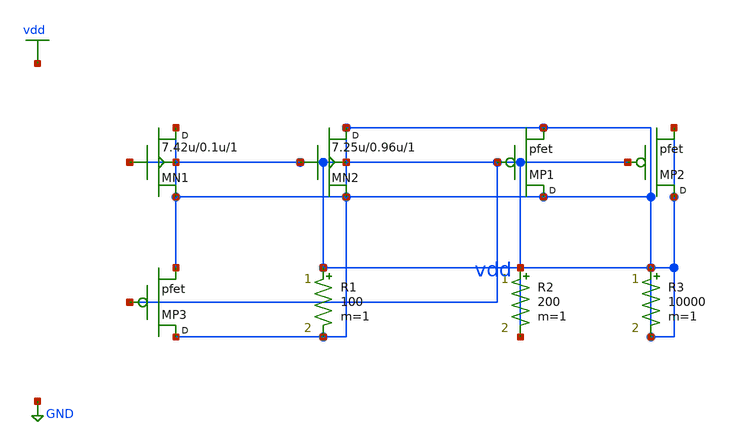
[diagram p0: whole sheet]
** sch_path: synthetic/generated/0039_synthetic.sch
**.subckt 0039_synthetic
MN1 vdd vdd vdd vdd nfet w=7.42u l=0.1u m=1
MN2 vdd vdd vdd vdd nfet w=7.25u l=0.96u m=1
MP1 vdd vdd vdd pfet m=1
MP2 vdd vdd vdd pfet m=1
MP3 vdd vdd vdd pfet m=1
R1 vdd vdd 100 m=1
R2 vdd vdd 200 m=1
R3 vdd vdd 10000 m=1
**.ends
.GLOBAL vdd
.GLOBAL GND
.end
